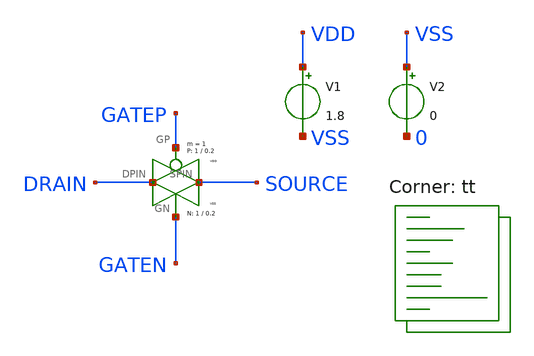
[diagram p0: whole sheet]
** sch_path: test-tg.sch
**.subckt test-tg
V1 VDD VSS 1.8
V2 VSS 0 0
x1 GATEP DRAIN SOURCE GATEN VDD VSS transmissiongate W_P=1 L_P=0.2 W_N=1 L_N=0.2 m=1
**** begin user architecture code
.lib $::SKYWATER_MODELS/sky130.lib.spice tt
**** end user architecture code
**.ends

* expanding   symbol:  transmissiongate.sym # of pins=4
** sym_path: transmissiongate.sym
** sch_path: transmissiongate.sch
.subckt transmissiongate GP DPIN SPIN GN VDDBPIN VSSBPIN  W_P=1 L_P=0.2 W_N=1 L_N=0.2
*.iopin DPIN
*.iopin SPIN
*.ipin GP
*.ipin GN
XM1 DPIN GN SPIN VSSBPIN sky130_fd_pr__nfet_01v8 L=L_N W=W_N nf=1 ad='int((nf+1)/2) * W/nf * 0.29' as='int((nf+2)/2) * W/nf * 0.29'
+ pd='2*int((nf+1)/2) * (W/nf + 0.29)' ps='2*int((nf+2)/2) * (W/nf + 0.29)' nrd='0.29 / W' nrs='0.29 / W'
+ sa=0 sb=0 sd=0 mult=m m=m
XM2 DPIN GP SPIN VDDBPIN sky130_fd_pr__pfet_01v8 L=L_P W=W_P nf=1 ad='int((nf+1)/2) * W/nf * 0.29' as='int((nf+2)/2) * W/nf * 0.29'
+ pd='2*int((nf+1)/2) * (W/nf + 0.29)' ps='2*int((nf+2)/2) * (W/nf + 0.29)' nrd='0.29 / W' nrs='0.29 / W'
+ sa=0 sb=0 sd=0 mult=m m=m
* noconn VDDBPIN
* noconn VSSBPIN
.ends

.end
